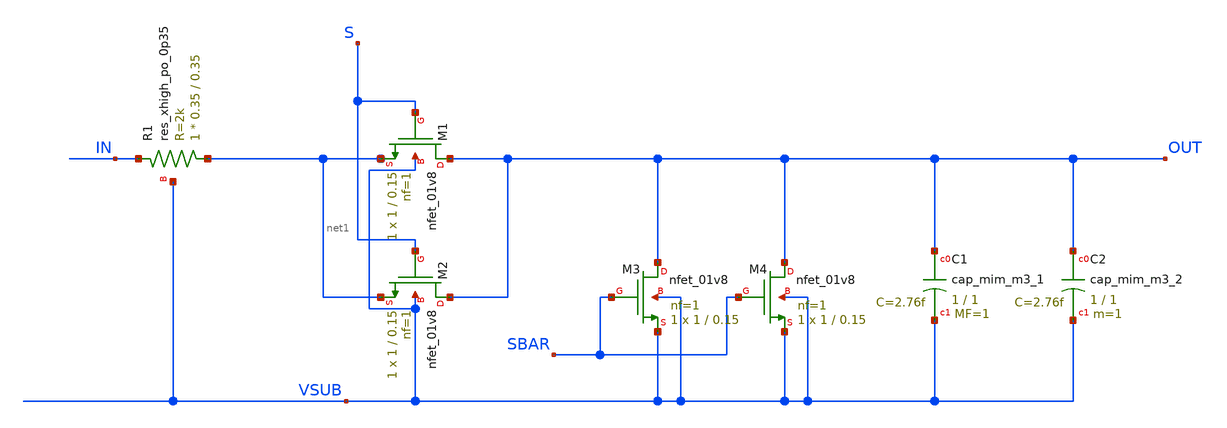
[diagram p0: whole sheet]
** sch_path: xschem/iref_gated_fix.sch
**.subckt iref_gated_fix
XM1 OUT S net1 VSUB sky130_fd_pr__nfet_01v8 L=0.15 W=1 nf=1 ad='int((nf+1)/2) * W/nf * 0.29' as='int((nf+2)/2) * W/nf * 0.29'
+ pd='2*int((nf+1)/2) * (W/nf + 0.29)' ps='2*int((nf+2)/2) * (W/nf + 0.29)' nrd='0.29 / W' nrs='0.29 / W'
+ sa=0 sb=0 sd=0 mult=1 m=1
XM2 OUT S net1 VSUB sky130_fd_pr__nfet_01v8 L=0.15 W=1 nf=1 ad='int((nf+1)/2) * W/nf * 0.29' as='int((nf+2)/2) * W/nf * 0.29'
+ pd='2*int((nf+1)/2) * (W/nf + 0.29)' ps='2*int((nf+2)/2) * (W/nf + 0.29)' nrd='0.29 / W' nrs='0.29 / W'
+ sa=0 sb=0 sd=0 mult=1 m=1
XM3 OUT SBAR VSUB VSUB sky130_fd_pr__nfet_01v8 L=0.15 W=1 nf=1 ad='int((nf+1)/2) * W/nf * 0.29' as='int((nf+2)/2) * W/nf * 0.29'
+ pd='2*int((nf+1)/2) * (W/nf + 0.29)' ps='2*int((nf+2)/2) * (W/nf + 0.29)' nrd='0.29 / W' nrs='0.29 / W'
+ sa=0 sb=0 sd=0 mult=1 m=1
XM4 OUT SBAR VSUB VSUB sky130_fd_pr__nfet_01v8 L=0.15 W=1 nf=1 ad='int((nf+1)/2) * W/nf * 0.29' as='int((nf+2)/2) * W/nf * 0.29'
+ pd='2*int((nf+1)/2) * (W/nf + 0.29)' ps='2*int((nf+2)/2) * (W/nf + 0.29)' nrd='0.29 / W' nrs='0.29 / W'
+ sa=0 sb=0 sd=0 mult=1 m=1
XR1 net1 IN VSUB sky130_fd_pr__res_xhigh_po_0p35 L=0.35 mult=1 m=1
XC1 OUT VSUB sky130_fd_pr__cap_mim_m3_1 W=1 L=1 MF=1 m=1
XC2 OUT VSUB sky130_fd_pr__cap_mim_m3_2 W=1 L=1 MF=1 m=1
**.ends
.end
